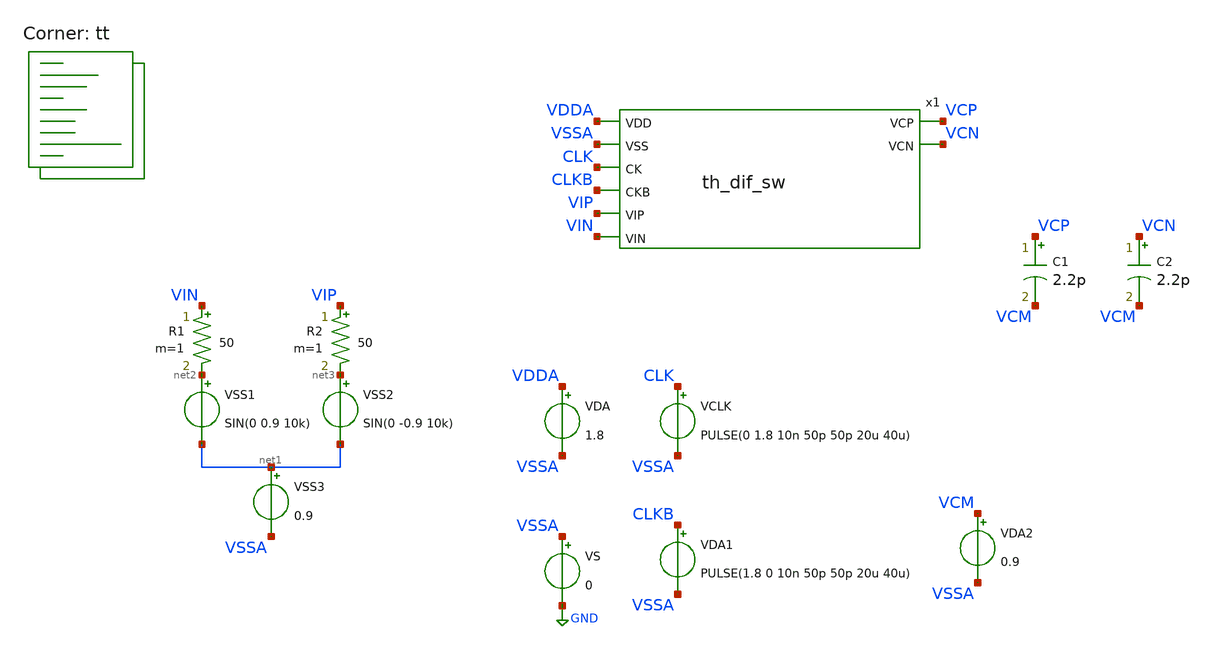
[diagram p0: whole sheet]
** sch_path: xschem/th_tb.sch
**.subckt th_tb
VS VSSA GND 0
VDA VDDA VSSA 1.8
VSS1 net2 net1 SIN(0 0.9 10k)
VSS2 net3 net1 SIN(0 -0.9 10k)
VSS3 net1 VSSA 0.9
VCLK CLK VSSA PULSE(0 1.8 10n 50p 50p 20u 40u)
R1 VIN net2 50 m=1
R2 VIP net3 50 m=1
VDA1 CLKB VSSA PULSE(1.8 0 10n 50p 50p 20u 40u)
x1 VDDA VSSA CLK CLKB VIP VIN VCP VCN th_dif_sw
C1 VCP VCM 2.2p m=1
C2 VCN VCM 2.2p m=1
VDA2 VCM VSSA 0.9
**** begin user architecture code

** opencircuitdesign pdks install
* .lib $::SKYWATER_MODELS/sky130.lib.spice tt
.include $PDK_ROOT/$PDK/libs.ref/sky130_fd_sc_hd/spice/sky130_fd_sc_hd.spice



.option wnflag=0
.option savecurrents
.options method=trapezoid
.options solver=iterative
.control
global netlist_dir .
set wr_singlescale
save vcp vcn vip vin clk clkb
tran 10n 1m  ; Mengubah start time menjadi 1n
remzerovec
write th_tb.raw
quit 0
.endc

.lib $::SKYWATER_MODELS/sky130.lib.spice tt
**** end user architecture code
**.ends

* expanding   symbol:  th_dif_sw.sym # of pins=8
** sym_path: th_dif_sw.sym
** sch_path: th_dif_sw.sch
.subckt th_dif_sw VDD VSS CK CKB VIP VIN VCP VCN
*.ipin VDD
*.ipin VSS
*.ipin CK
*.ipin CKB
*.ipin VIP
*.ipin VIN
*.opin VCP
*.opin VCN
x1 VDD VSS CK CKB VIP VCP th_sw
x2 VDD VSS CK CKB VIN VCN th_sw
.ends


* expanding   symbol:  th_sw.sym # of pins=6
** sym_path: th_sw.sym
** sch_path: th_sw.sch
.subckt th_sw VDD VSS CK CKB IN OUT
*.ipin VDD
*.ipin VSS
*.ipin CK
*.ipin CKB
*.ipin IN
*.opin OUT
XM1 net1 CKB VDD VDD sky130_fd_pr__pfet_01v8 L=0.15 W=3 nf=1 ad='int((nf+1)/2) * W/nf * 0.29' as='int((nf+2)/2) * W/nf * 0.29'
+ pd='2*int((nf+1)/2) * (W/nf + 0.29)' ps='2*int((nf+2)/2) * (W/nf + 0.29)' nrd='0.29 / W' nrs='0.29 / W'
+ sa=0 sb=0 sd=0 mult=1 m=1
XM2 net2 net3 VDD net2 sky130_fd_pr__pfet_01v8 L=0.15 W=3 nf=1 ad='int((nf+1)/2) * W/nf * 0.29' as='int((nf+2)/2) * W/nf * 0.29'
+ pd='2*int((nf+1)/2) * (W/nf + 0.29)' ps='2*int((nf+2)/2) * (W/nf + 0.29)' nrd='0.29 / W' nrs='0.29 / W'
+ sa=0 sb=0 sd=0 mult=1 m=1
XM3 net3 net1 net2 net2 sky130_fd_pr__pfet_01v8 L=0.15 W=3 nf=1 ad='int((nf+1)/2) * W/nf * 0.29' as='int((nf+2)/2) * W/nf * 0.29'
+ pd='2*int((nf+1)/2) * (W/nf + 0.29)' ps='2*int((nf+2)/2) * (W/nf + 0.29)' nrd='0.29 / W' nrs='0.29 / W'
+ sa=0 sb=0 sd=0 mult=1 m=1
XM4 net1 CKB net5 VSS sky130_fd_pr__nfet_01v8 L=0.15 W=1 nf=1 ad='int((nf+1)/2) * W/nf * 0.29' as='int((nf+2)/2) * W/nf * 0.29'
+ pd='2*int((nf+1)/2) * (W/nf + 0.29)' ps='2*int((nf+2)/2) * (W/nf + 0.29)' nrd='0.29 / W' nrs='0.29 / W'
+ sa=0 sb=0 sd=0 mult=1 m=1
XM5 net5 CK VSS VSS sky130_fd_pr__nfet_01v8 L=0.15 W=1 nf=1 ad='int((nf+1)/2) * W/nf * 0.29' as='int((nf+2)/2) * W/nf * 0.29'
+ pd='2*int((nf+1)/2) * (W/nf + 0.29)' ps='2*int((nf+2)/2) * (W/nf + 0.29)' nrd='0.29 / W' nrs='0.29 / W'
+ sa=0 sb=0 sd=0 mult=1 m=1
XM6 net1 net3 net5 VSS sky130_fd_pr__nfet_01v8 L=0.15 W=1 nf=1 ad='int((nf+1)/2) * W/nf * 0.29' as='int((nf+2)/2) * W/nf * 0.29'
+ pd='2*int((nf+1)/2) * (W/nf + 0.29)' ps='2*int((nf+2)/2) * (W/nf + 0.29)' nrd='0.29 / W' nrs='0.29 / W'
+ sa=0 sb=0 sd=0 mult=1 m=1
XM7 net5 net3 IN VSS sky130_fd_pr__nfet_01v8 L=0.15 W=1 nf=1 ad='int((nf+1)/2) * W/nf * 0.29' as='int((nf+2)/2) * W/nf * 0.29'
+ pd='2*int((nf+1)/2) * (W/nf + 0.29)' ps='2*int((nf+2)/2) * (W/nf + 0.29)' nrd='0.29 / W' nrs='0.29 / W'
+ sa=0 sb=0 sd=0 mult=1 m=1
XM8 net3 VDD net4 VSS sky130_fd_pr__nfet_01v8 L=0.15 W=1 nf=1 ad='int((nf+1)/2) * W/nf * 0.29' as='int((nf+2)/2) * W/nf * 0.29'
+ pd='2*int((nf+1)/2) * (W/nf + 0.29)' ps='2*int((nf+2)/2) * (W/nf + 0.29)' nrd='0.29 / W' nrs='0.29 / W'
+ sa=0 sb=0 sd=0 mult=1 m=1
XM9 net4 CK VSS VSS sky130_fd_pr__nfet_01v8 L=0.15 W=1 nf=1 ad='int((nf+1)/2) * W/nf * 0.29' as='int((nf+2)/2) * W/nf * 0.29'
+ pd='2*int((nf+1)/2) * (W/nf + 0.29)' ps='2*int((nf+2)/2) * (W/nf + 0.29)' nrd='0.29 / W' nrs='0.29 / W'
+ sa=0 sb=0 sd=0 mult=1 m=1
XC1 net2 net5 sky130_fd_pr__cap_mim_m3_1 W=2 L=2 MF=4 m=4
XM10 OUT net3 IN VSS sky130_fd_pr__nfet_01v8 L=0.5 W=8 nf=1 ad='int((nf+1)/2) * W/nf * 0.29' as='int((nf+2)/2) * W/nf * 0.29'
+ pd='2*int((nf+1)/2) * (W/nf + 0.29)' ps='2*int((nf+2)/2) * (W/nf + 0.29)' nrd='0.29 / W' nrs='0.29 / W'
+ sa=0 sb=0 sd=0 mult=1 m=1
.ends

.GLOBAL GND
.end
